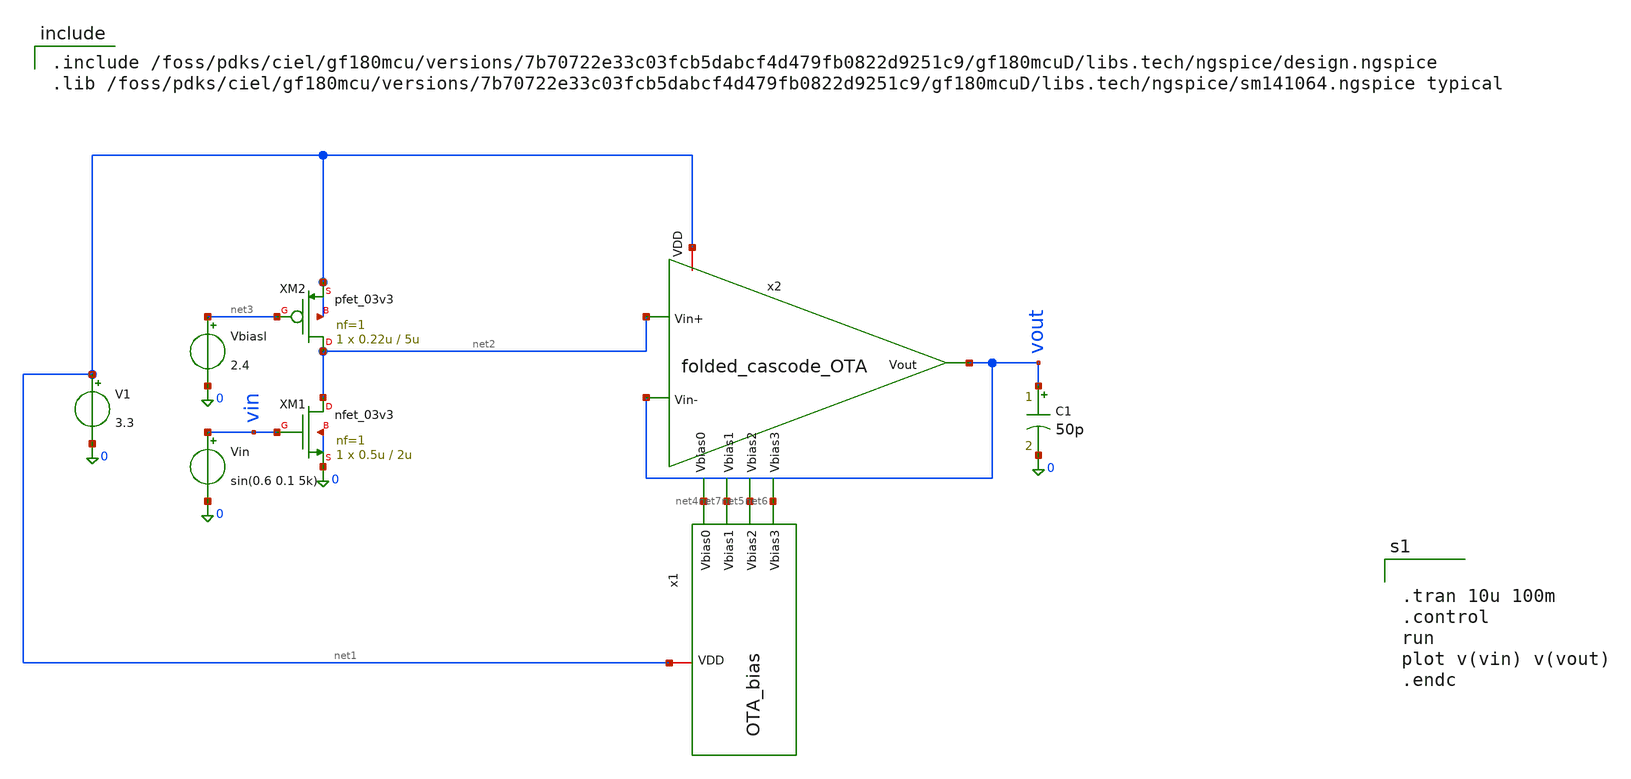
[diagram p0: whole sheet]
** sch_path: analog/envelope_detector.sch
**.subckt envelope_detector
XM1 net2 vin 0 0 nfet_03v3 L=2u W=0.5u nf=1 ad='int((nf+1)/2) * W/nf * 0.18u' as='int((nf+2)/2) * W/nf * 0.18u'
+ pd='2*int((nf+1)/2) * (W/nf + 0.18u)' ps='2*int((nf+2)/2) * (W/nf + 0.18u)' nrd='0.18u / W' nrs='0.18u / W'
+ sa=0 sb=0 sd=0 m=1
XM2 net2 net3 net1 net1 pfet_03v3 L=5u W=0.22u nf=1 ad='int((nf+1)/2) * W/nf * 0.18u' as='int((nf+2)/2) * W/nf * 0.18u'
+ pd='2*int((nf+1)/2) * (W/nf + 0.18u)' ps='2*int((nf+2)/2) * (W/nf + 0.18u)' nrd='0.18u / W' nrs='0.18u / W'
+ sa=0 sb=0 sd=0 m=1
x1 net1 net4 net5 net6 net7 OTA_bias
x2 net1 net4 net2 vout net6 net7 vout net5 folded_cascode_OTA
V1 net1 0 3.3
Vin vin 0 sin(0.6 0.1 5k)
Vbiasl net3 0 2.4
C1 vout 0 50p m=1
**** begin user architecture code

.include /foss/pdks/ciel/gf180mcu/versions/7b70722e33c03fcb5dabcf4d479fb0822d9251c9/gf180mcuD/libs.tech/ngspice/design.ngspice
.lib /foss/pdks/ciel/gf180mcu/versions/7b70722e33c03fcb5dabcf4d479fb0822d9251c9/gf180mcuD/libs.tech/ngspice/sm141064.ngspice typical



.tran 10u 100m
.control
run
plot v(vin) v(vout)
.endc


**** end user architecture code
**.ends

* expanding   symbol:  AURA/OTA_bias.sym # of pins=5
** sym_path: analog/OTA_bias.sym
** sch_path: analog/OTA_bias.sch
.subckt OTA_bias VDD Vbias0 Vbias2 Vbias3 Vbias1
*.iopin VDD
*.opin Vbias2
*.opin Vbias1
*.opin Vbias0
*.opin Vbias3
**** begin user architecture code

.include /foss/pdks/ciel/gf180mcu/versions/7b70722e33c03fcb5dabcf4d479fb0822d9251c9/gf180mcuD/libs.tech/ngspice/design.ngspice
.lib /foss/pdks/ciel/gf180mcu/versions/7b70722e33c03fcb5dabcf4d479fb0822d9251c9/gf180mcuD/libs.tech/ngspice/sm141064.ngspice typical

**** end user architecture code
XM1 Vbias1 0 Vbias2 VDD pfet_03v3 L=1u W=2u nf=1 ad='int((nf+1)/2) * W/nf * 0.18u' as='int((nf+2)/2) * W/nf * 0.18u'
+ pd='2*int((nf+1)/2) * (W/nf + 0.18u)' ps='2*int((nf+2)/2) * (W/nf + 0.18u)' nrd='0.18u / W' nrs='0.18u / W'
+ sa=0 sb=0 sd=0 m=1
XM4 Vbias1 Vbias2 net1 0 nfet_03v3 L=1u W=2u nf=1 ad='int((nf+1)/2) * W/nf * 0.18u' as='int((nf+2)/2) * W/nf * 0.18u'
+ pd='2*int((nf+1)/2) * (W/nf + 0.18u)' ps='2*int((nf+2)/2) * (W/nf + 0.18u)' nrd='0.18u / W' nrs='0.18u / W'
+ sa=0 sb=0 sd=0 m=1
XM5 net1 Vbias1 0 0 nfet_03v3 L=1u W=2u nf=1 ad='int((nf+1)/2) * W/nf * 0.18u' as='int((nf+2)/2) * W/nf * 0.18u'
+ pd='2*int((nf+1)/2) * (W/nf + 0.18u)' ps='2*int((nf+2)/2) * (W/nf + 0.18u)' nrd='0.18u / W' nrs='0.18u / W'
+ sa=0 sb=0 sd=0 m=1
XM9 net2 Vbias3 Vbias0 VDD pfet_03v3 L=1u W=2u nf=1 ad='int((nf+1)/2) * W/nf * 0.18u' as='int((nf+2)/2) * W/nf * 0.18u'
+ pd='2*int((nf+1)/2) * (W/nf + 0.18u)' ps='2*int((nf+2)/2) * (W/nf + 0.18u)' nrd='0.18u / W' nrs='0.18u / W'
+ sa=0 sb=0 sd=0 m=1
XM10 VDD Vbias0 net2 VDD pfet_03v3 L=1u W=2u nf=1 ad='int((nf+1)/2) * W/nf * 0.18u' as='int((nf+2)/2) * W/nf * 0.18u'
+ pd='2*int((nf+1)/2) * (W/nf + 0.18u)' ps='2*int((nf+2)/2) * (W/nf + 0.18u)' nrd='0.18u / W' nrs='0.18u / W'
+ sa=0 sb=0 sd=0 m=1
XM6 Vbias3 VDD Vbias0 0 nfet_03v3 L=1u W=2u nf=1 ad='int((nf+1)/2) * W/nf * 0.18u' as='int((nf+2)/2) * W/nf * 0.18u'
+ pd='2*int((nf+1)/2) * (W/nf + 0.18u)' ps='2*int((nf+2)/2) * (W/nf + 0.18u)' nrd='0.18u / W' nrs='0.18u / W'
+ sa=0 sb=0 sd=0 m=1
I0 VDD Vbias2 200n
I1 Vbias3 0 200n
.ends


* expanding   symbol:  AURA/folded_cascode_OTA.sym # of pins=8
** sym_path: analog/folded_cascode_OTA.sym
** sch_path: analog/folded_cascode_OTA.sch
.subckt folded_cascode_OTA VDD Vbias0 Vin+ Vin- Vbias3 Vbias1 Vout Vbias2
*.iopin VDD
*.ipin Vbias0
*.ipin Vin+
*.ipin Vin-
*.ipin Vbias1
*.opin Vout
*.ipin Vbias3
*.ipin Vbias2
XM1 net1 Vbias0 VDD VDD pfet_03v3 L=1u W=2u nf=2 ad='int((nf+1)/2) * W/nf * 0.18u' as='int((nf+2)/2) * W/nf * 0.18u'
+ pd='2*int((nf+1)/2) * (W/nf + 0.18u)' ps='2*int((nf+2)/2) * (W/nf + 0.18u)' nrd='0.18u / W' nrs='0.18u / W'
+ sa=0 sb=0 sd=0 m=1
XM2 net6 Vin+ net1 net1 pfet_03v3 L=1u W=2u nf=9 ad='int((nf+1)/2) * W/nf * 0.18u' as='int((nf+2)/2) * W/nf * 0.18u'
+ pd='2*int((nf+1)/2) * (W/nf + 0.18u)' ps='2*int((nf+2)/2) * (W/nf + 0.18u)' nrd='0.18u / W' nrs='0.18u / W'
+ sa=0 sb=0 sd=0 m=1
XM3 net7 Vin- net1 net1 pfet_03v3 L=1u W=2u nf=9 ad='int((nf+1)/2) * W/nf * 0.18u' as='int((nf+2)/2) * W/nf * 0.18u'
+ pd='2*int((nf+1)/2) * (W/nf + 0.18u)' ps='2*int((nf+2)/2) * (W/nf + 0.18u)' nrd='0.18u / W' nrs='0.18u / W'
+ sa=0 sb=0 sd=0 m=1
XM4 net2 Vin+ net1 net1 pfet_03v3 L=1u W=2u nf=1 ad='int((nf+1)/2) * W/nf * 0.18u' as='int((nf+2)/2) * W/nf * 0.18u'
+ pd='2*int((nf+1)/2) * (W/nf + 0.18u)' ps='2*int((nf+2)/2) * (W/nf + 0.18u)' nrd='0.18u / W' nrs='0.18u / W'
+ sa=0 sb=0 sd=0 m=1
XM5 net3 Vin- net1 net1 pfet_03v3 L=1u W=2u nf=1 ad='int((nf+1)/2) * W/nf * 0.18u' as='int((nf+2)/2) * W/nf * 0.18u'
+ pd='2*int((nf+1)/2) * (W/nf + 0.18u)' ps='2*int((nf+2)/2) * (W/nf + 0.18u)' nrd='0.18u / W' nrs='0.18u / W'
+ sa=0 sb=0 sd=0 m=1
XM6 net2 Vbias2 net5 0 nfet_03v3 L=1u W=2u nf=1 ad='int((nf+1)/2) * W/nf * 0.18u' as='int((nf+2)/2) * W/nf * 0.18u'
+ pd='2*int((nf+1)/2) * (W/nf + 0.18u)' ps='2*int((nf+2)/2) * (W/nf + 0.18u)' nrd='0.18u / W' nrs='0.18u / W'
+ sa=0 sb=0 sd=0 m=1
XM7 net3 Vbias2 net4 0 nfet_03v3 L=1u W=2u nf=1 ad='int((nf+1)/2) * W/nf * 0.18u' as='int((nf+2)/2) * W/nf * 0.18u'
+ pd='2*int((nf+1)/2) * (W/nf + 0.18u)' ps='2*int((nf+2)/2) * (W/nf + 0.18u)' nrd='0.18u / W' nrs='0.18u / W'
+ sa=0 sb=0 sd=0 m=1
XM8 net5 net2 0 0 nfet_03v3 L=2u W=2u nf=1 ad='int((nf+1)/2) * W/nf * 0.18u' as='int((nf+2)/2) * W/nf * 0.18u'
+ pd='2*int((nf+1)/2) * (W/nf + 0.18u)' ps='2*int((nf+2)/2) * (W/nf + 0.18u)' nrd='0.18u / W' nrs='0.18u / W'
+ sa=0 sb=0 sd=0 m=1
XM9 net6 net3 0 0 nfet_03v3 L=2u W=2u nf=1 ad='int((nf+1)/2) * W/nf * 0.18u' as='int((nf+2)/2) * W/nf * 0.18u'
+ pd='2*int((nf+1)/2) * (W/nf + 0.18u)' ps='2*int((nf+2)/2) * (W/nf + 0.18u)' nrd='0.18u / W' nrs='0.18u / W'
+ sa=0 sb=0 sd=0 m=1
XM10 net4 net3 0 0 nfet_03v3 L=2u W=2u nf=1 ad='int((nf+1)/2) * W/nf * 0.18u' as='int((nf+2)/2) * W/nf * 0.18u'
+ pd='2*int((nf+1)/2) * (W/nf + 0.18u)' ps='2*int((nf+2)/2) * (W/nf + 0.18u)' nrd='0.18u / W' nrs='0.18u / W'
+ sa=0 sb=0 sd=0 m=1
XM11 net7 net2 0 0 nfet_03v3 L=2u W=2u nf=1 ad='int((nf+1)/2) * W/nf * 0.18u' as='int((nf+2)/2) * W/nf * 0.18u'
+ pd='2*int((nf+1)/2) * (W/nf + 0.18u)' ps='2*int((nf+2)/2) * (W/nf + 0.18u)' nrd='0.18u / W' nrs='0.18u / W'
+ sa=0 sb=0 sd=0 m=1
XM12 net9 net10 VDD VDD pfet_03v3 L=1u W=2u nf=1 ad='int((nf+1)/2) * W/nf * 0.18u' as='int((nf+2)/2) * W/nf * 0.18u'
+ pd='2*int((nf+1)/2) * (W/nf + 0.18u)' ps='2*int((nf+2)/2) * (W/nf + 0.18u)' nrd='0.18u / W' nrs='0.18u / W'
+ sa=0 sb=0 sd=0 m=1
XM13 net8 net10 VDD VDD pfet_03v3 L=1u W=2u nf=1 ad='int((nf+1)/2) * W/nf * 0.18u' as='int((nf+2)/2) * W/nf * 0.18u'
+ pd='2*int((nf+1)/2) * (W/nf + 0.18u)' ps='2*int((nf+2)/2) * (W/nf + 0.18u)' nrd='0.18u / W' nrs='0.18u / W'
+ sa=0 sb=0 sd=0 m=1
XM14 Vout Vbias3 net9 net9 pfet_03v3 L=1u W=2u nf=1 ad='int((nf+1)/2) * W/nf * 0.18u' as='int((nf+2)/2) * W/nf * 0.18u'
+ pd='2*int((nf+1)/2) * (W/nf + 0.18u)' ps='2*int((nf+2)/2) * (W/nf + 0.18u)' nrd='0.18u / W' nrs='0.18u / W'
+ sa=0 sb=0 sd=0 m=1
XM15 net10 Vbias3 net8 net8 pfet_03v3 L=1u W=2u nf=1 ad='int((nf+1)/2) * W/nf * 0.18u' as='int((nf+2)/2) * W/nf * 0.18u'
+ pd='2*int((nf+1)/2) * (W/nf + 0.18u)' ps='2*int((nf+2)/2) * (W/nf + 0.18u)' nrd='0.18u / W' nrs='0.18u / W'
+ sa=0 sb=0 sd=0 m=1
XM16 Vout Vbias1 net7 0 nfet_03v3 L=1u W=2u nf=1 ad='int((nf+1)/2) * W/nf * 0.18u' as='int((nf+2)/2) * W/nf * 0.18u'
+ pd='2*int((nf+1)/2) * (W/nf + 0.18u)' ps='2*int((nf+2)/2) * (W/nf + 0.18u)' nrd='0.18u / W' nrs='0.18u / W'
+ sa=0 sb=0 sd=0 m=1
XM17 net10 Vbias1 net6 0 nfet_03v3 L=1u W=2u nf=1 ad='int((nf+1)/2) * W/nf * 0.18u' as='int((nf+2)/2) * W/nf * 0.18u'
+ pd='2*int((nf+1)/2) * (W/nf + 0.18u)' ps='2*int((nf+2)/2) * (W/nf + 0.18u)' nrd='0.18u / W' nrs='0.18u / W'
+ sa=0 sb=0 sd=0 m=1
.ends

.end
